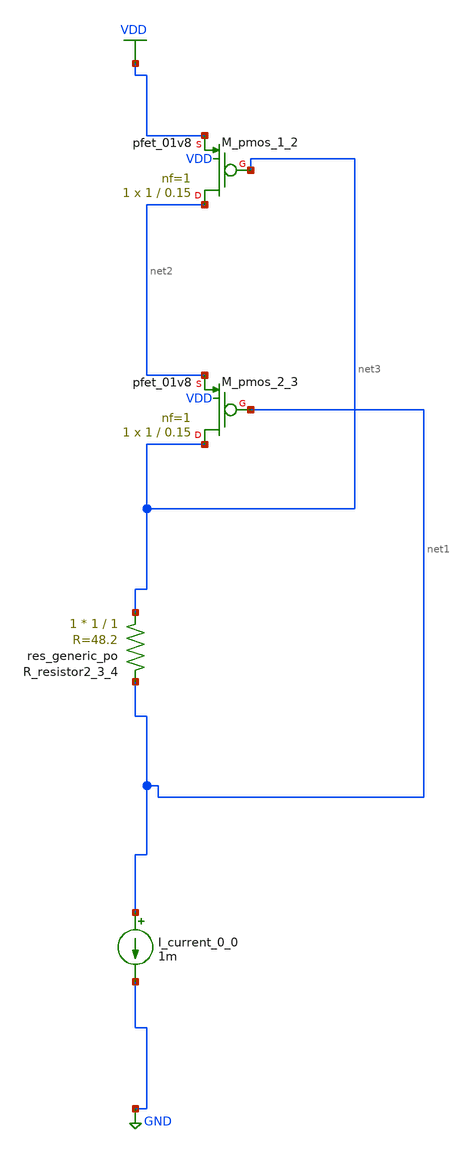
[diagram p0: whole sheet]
** sch_path: schematics/AMSNet/770.sch
**.subckt 770
I_current_0_0 net1 GND 1m
XM_pmos_1_2 net2 net3 VDD VDD sky130_fd_pr__pfet_01v8 L=0.15 W=1 nf=1 ad='int((1 + 1)/2) * 1 / 1 * 0.29'
+ as='int((1 + 2)/2) * 1 / 1 * 0.29' pd='2*int((1 + 1)/2) * (1 / 1 + 0.29)' ps='2*int((1 + 2)/2) * (1 / 1 + 0.29)'
+ nrd='0.29 / 1 ' nrs='0.29 / 1 ' sa=0 sb=0 sd=0 mult=1 m=1
XM_pmos_2_3 net3 net1 net2 VDD sky130_fd_pr__pfet_01v8 L=0.15 W=1 nf=1 ad='int((1 + 1)/2) * 1 / 1 * 0.29'
+ as='int((1 + 2)/2) * 1 / 1 * 0.29' pd='2*int((1 + 1)/2) * (1 / 1 + 0.29)' ps='2*int((1 + 2)/2) * (1 / 1 + 0.29)'
+ nrd='0.29 / 1 ' nrs='0.29 / 1 ' sa=0 sb=0 sd=0 mult=1 m=1
XR_resistor2_3_4 net3 net1 sky130_fd_pr__res_generic_po W=1 L=1 m=1
**.ends
.GLOBAL GND
.GLOBAL VDD
.end
